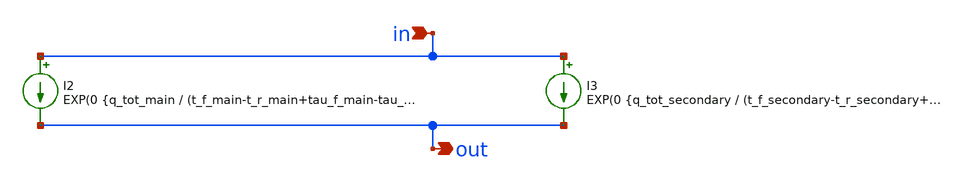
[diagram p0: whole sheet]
** sch_path: xschem_rad_library/dual_double_exp.sch
**.subckt dual_double_exp in out
*.ipin in
*.opin out
I2 in out EXP(0 {q_tot_main / (t_f_main-t_r_main+tau_f_main-tau_r_main)} {t_r_main} {tau_r_main} {t_f_main}
+ {tau_f_main})
I3 in out EXP(0 {q_tot_secondary / (t_f_secondary-t_r_secondary+tau_f_secondary-tau_r_secondary)} {t_r_secondary}
+ {tau_r_secondary} {t_f_secondary} {tau_f_secondary})
**.ends
.end
